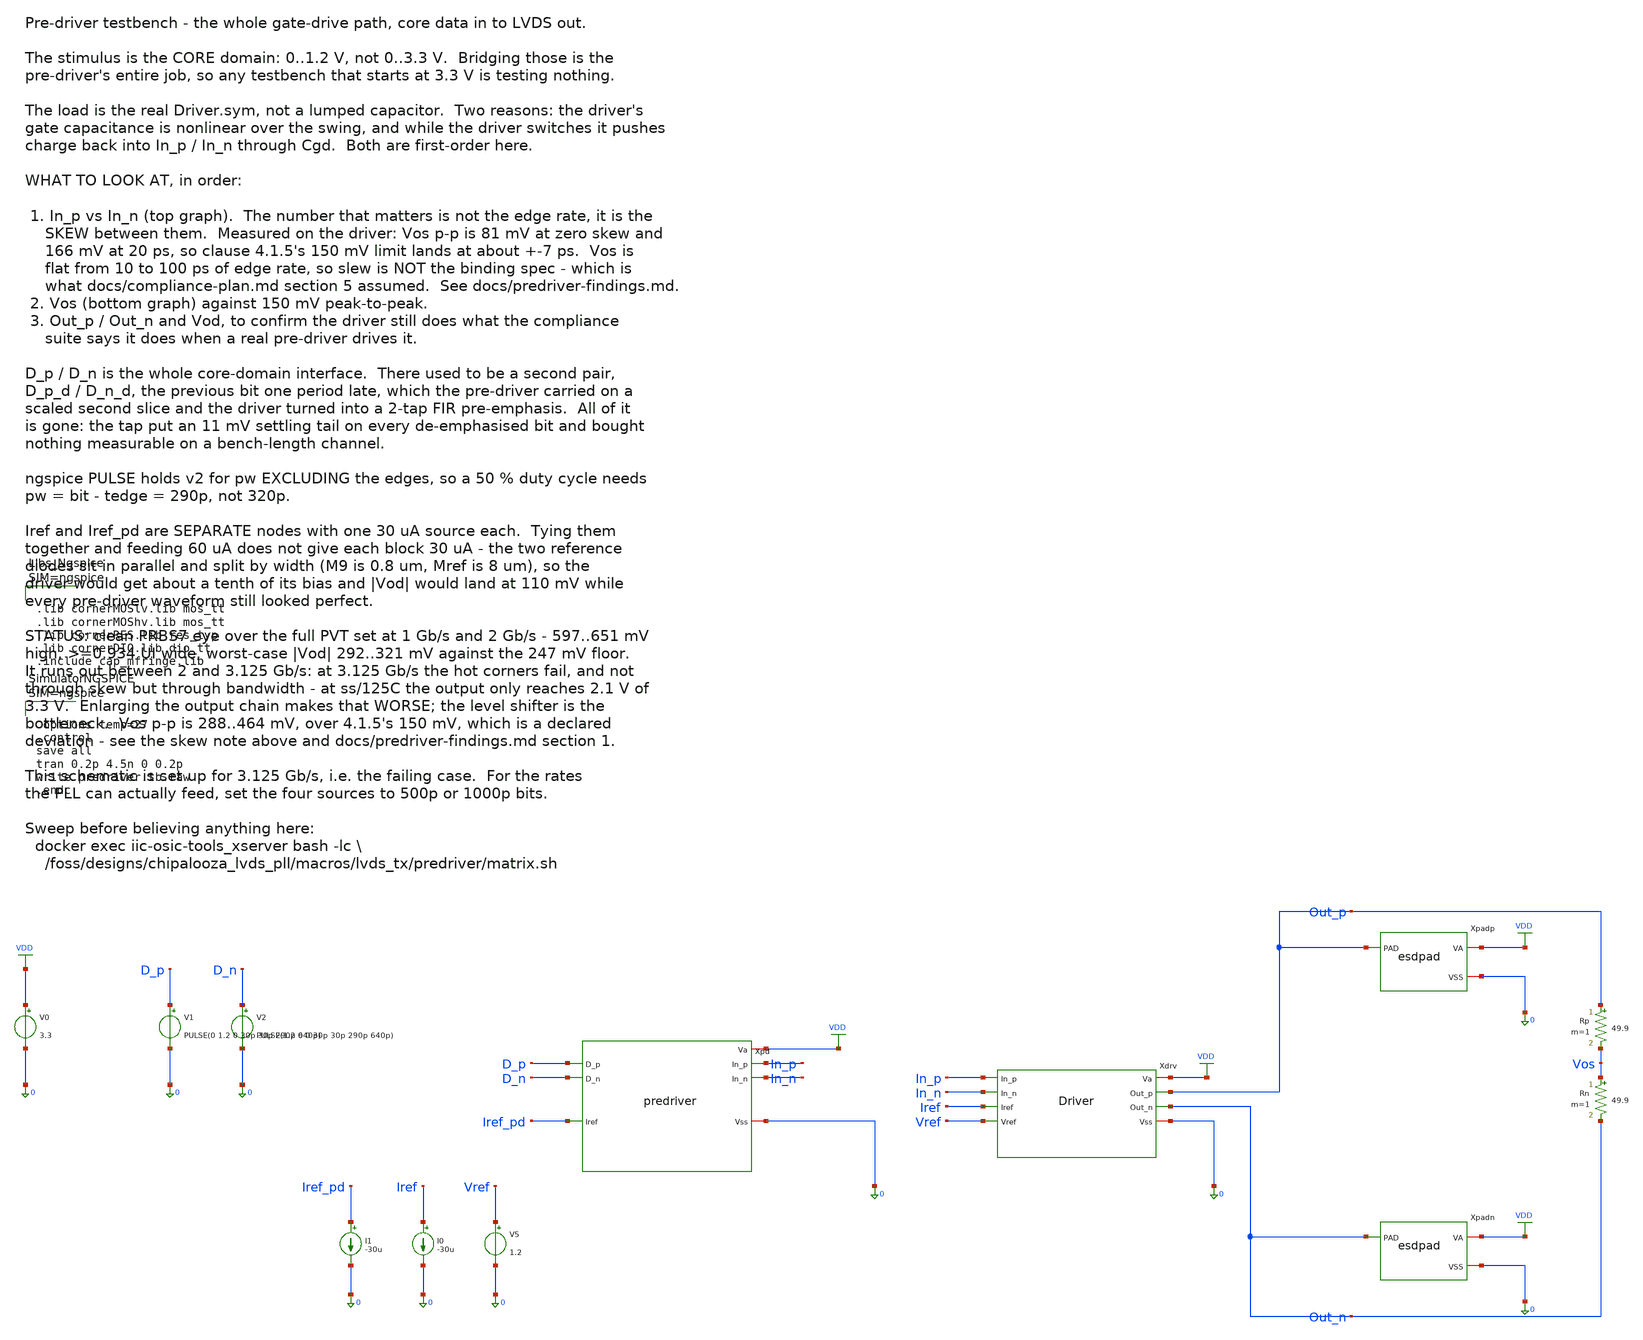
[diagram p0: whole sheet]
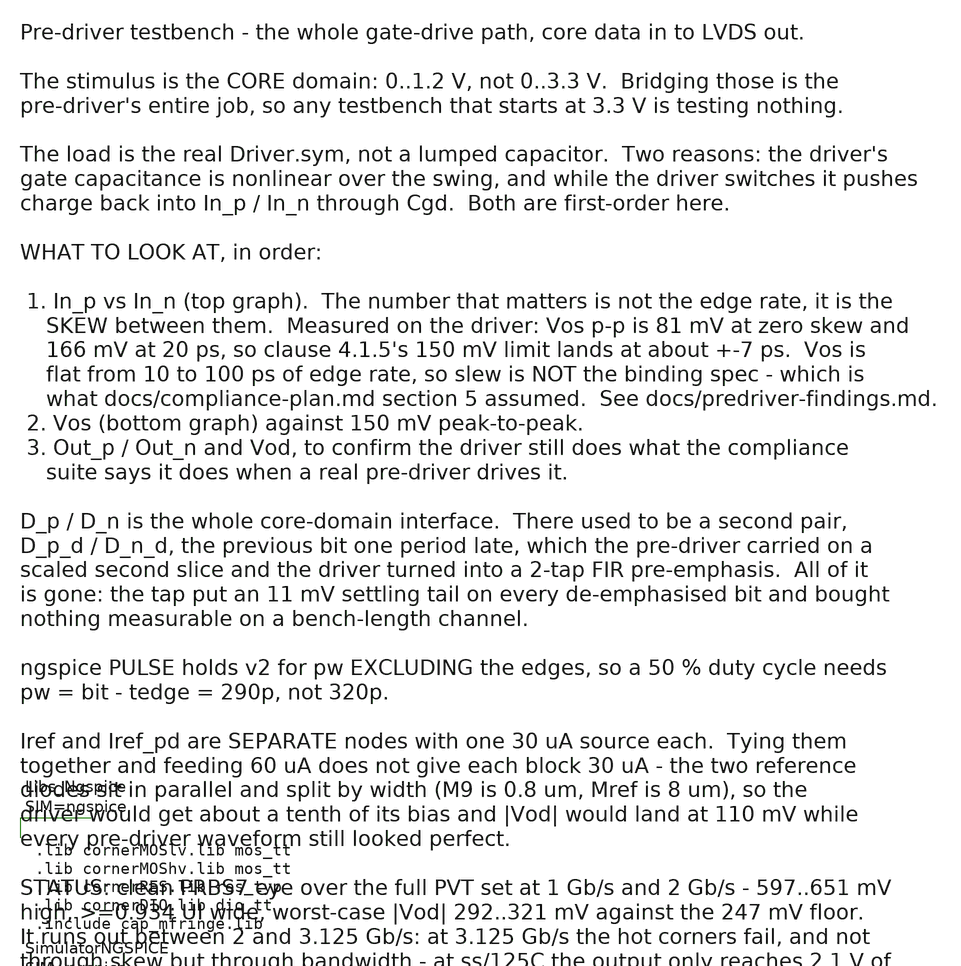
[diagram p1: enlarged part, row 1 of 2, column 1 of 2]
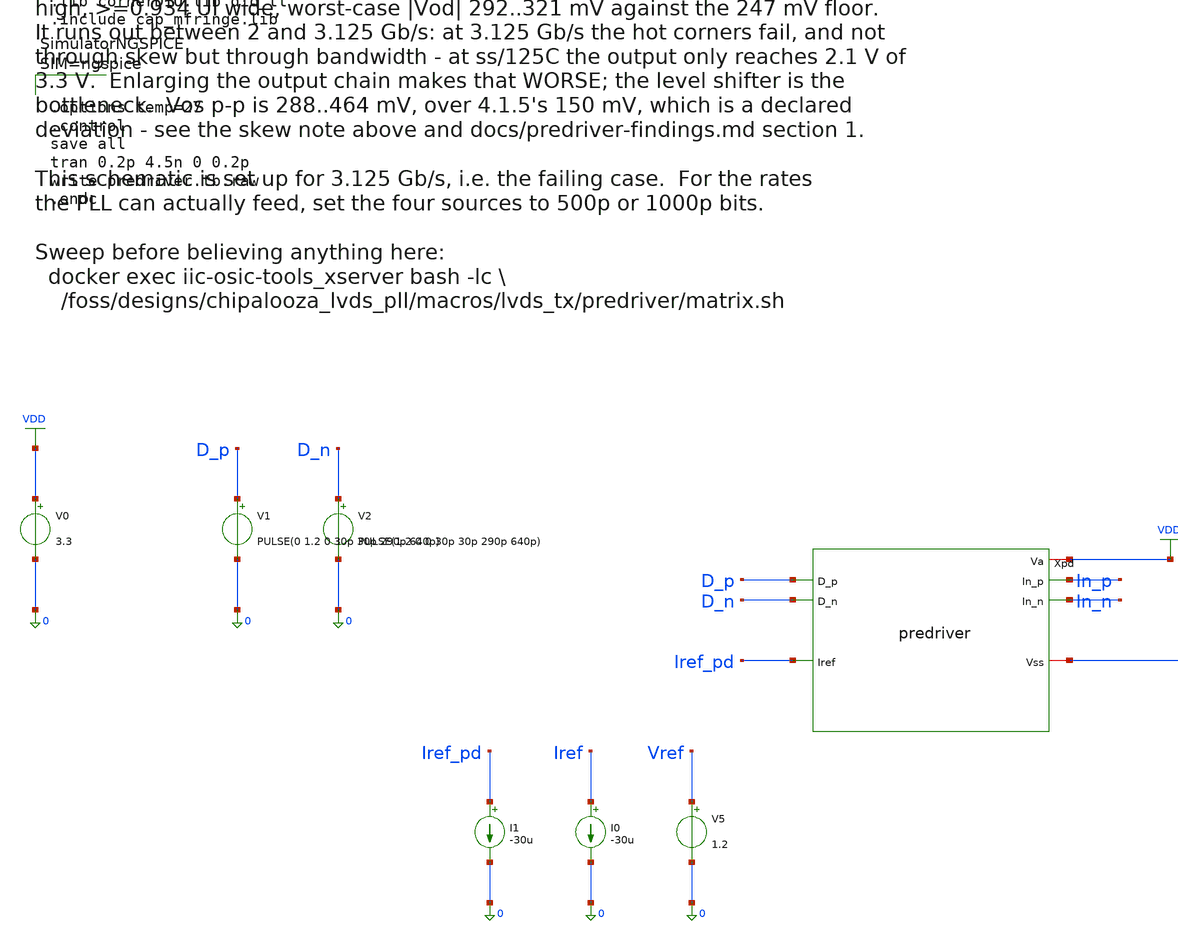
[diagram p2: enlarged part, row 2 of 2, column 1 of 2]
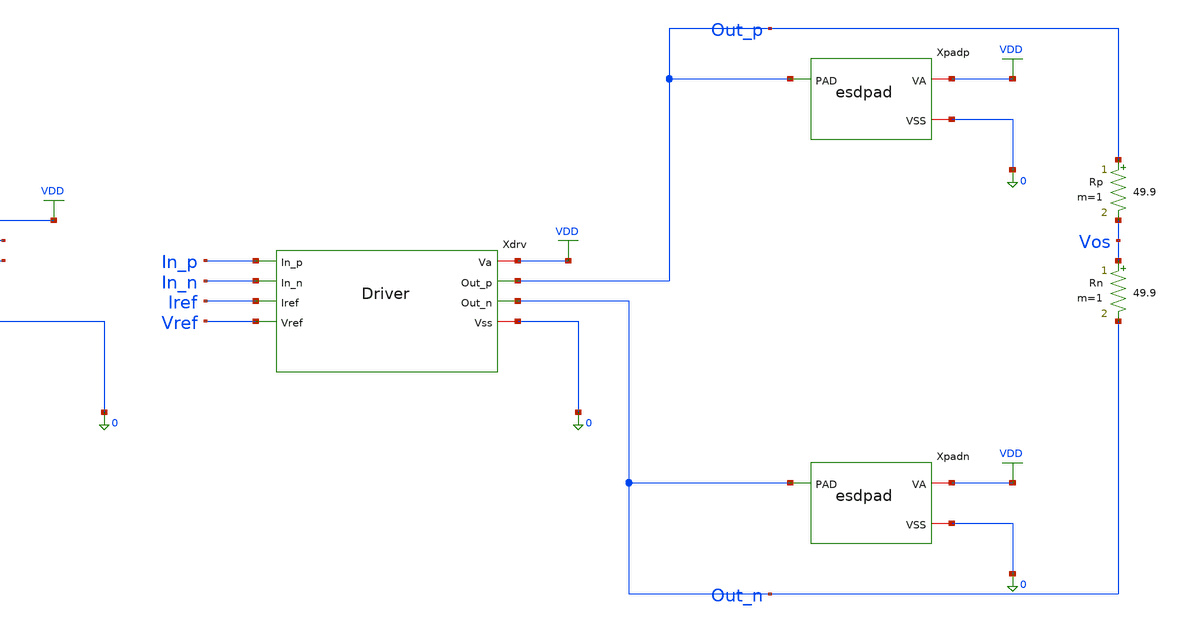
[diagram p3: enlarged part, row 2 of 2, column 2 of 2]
** sch_path: macros/lvds_tx/testbenches/xschem/predriver.tb.sch
**.subckt predriver.tb
Xpd D_p D_n Iref_pd In_p In_n VDD 0 predriver
Xdrv VDD Out_p In_p In_n Iref Vref Out_n 0 Driver
Xpadp Out_p VDD 0 esdpad
Xpadn Out_n VDD 0 esdpad
V0 VDD 0 3.3
V1 D_p 0 PULSE(0 1.2 0 30p 30p 290p 640p)
V2 D_n 0 PULSE(1.2 0 0 30p 30p 290p 640p)
V5 Vref 0 1.2
I0 Iref 0 -30u
I1 Iref_pd 0 -30u
Rp Out_p Vos 49.9 m=1
Rn Vos Out_n 49.9 m=1
**** begin user architecture code



.lib cornerMOSlv.lib mos_tt
.lib cornerMOShv.lib mos_tt
.lib cornerRES.lib res_typ
.lib cornerDIO.lib dio_tt
.include cap_mfringe.lib






.options temp=27
.control
save all
tran 0.2p 4.5n 0 0.2p
write predriver.tb.raw
.endc



**** end user architecture code
**.ends
.GLOBAL VDD
.end
